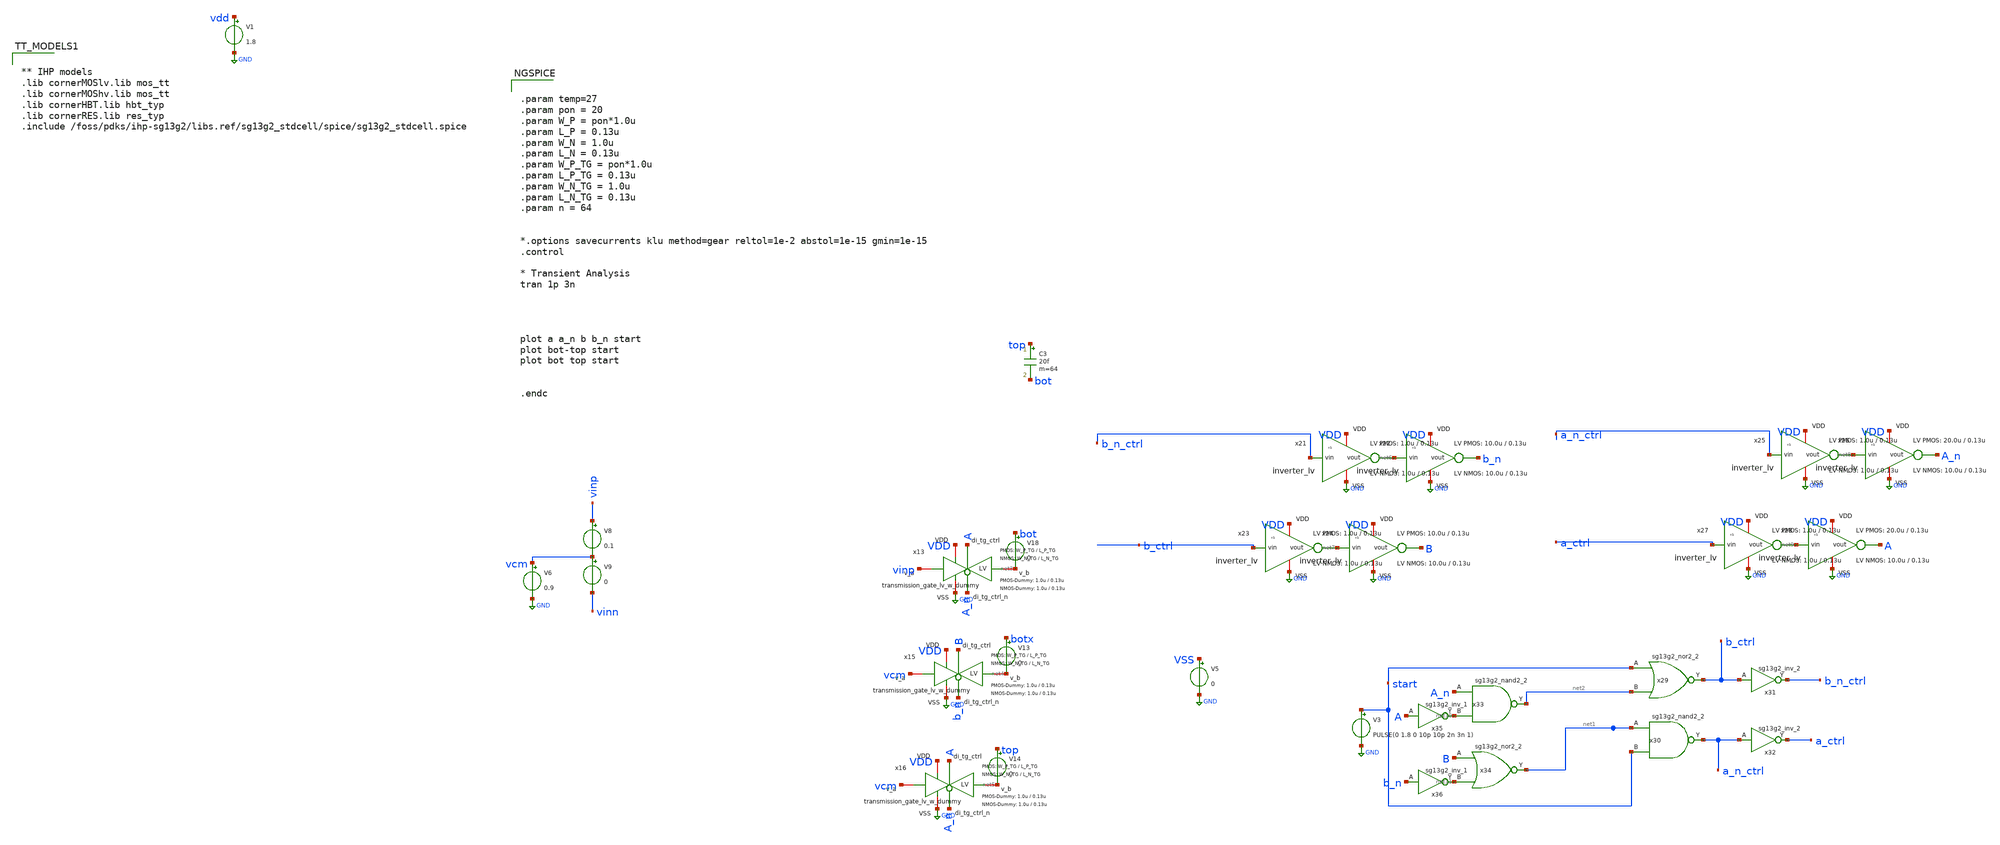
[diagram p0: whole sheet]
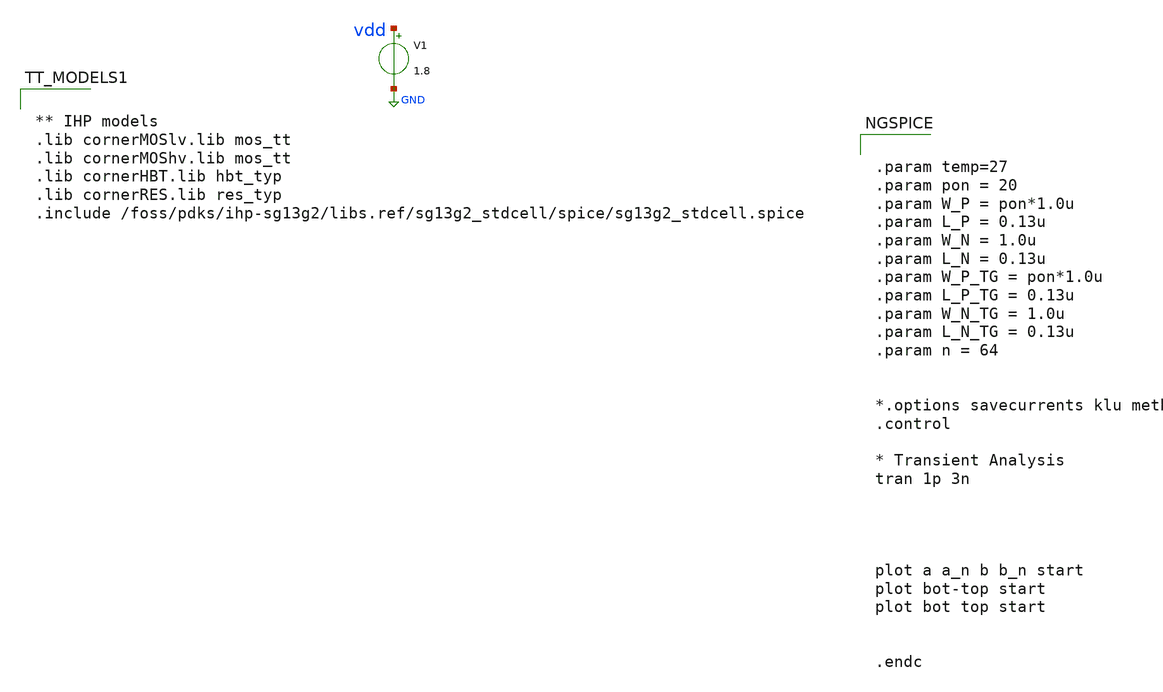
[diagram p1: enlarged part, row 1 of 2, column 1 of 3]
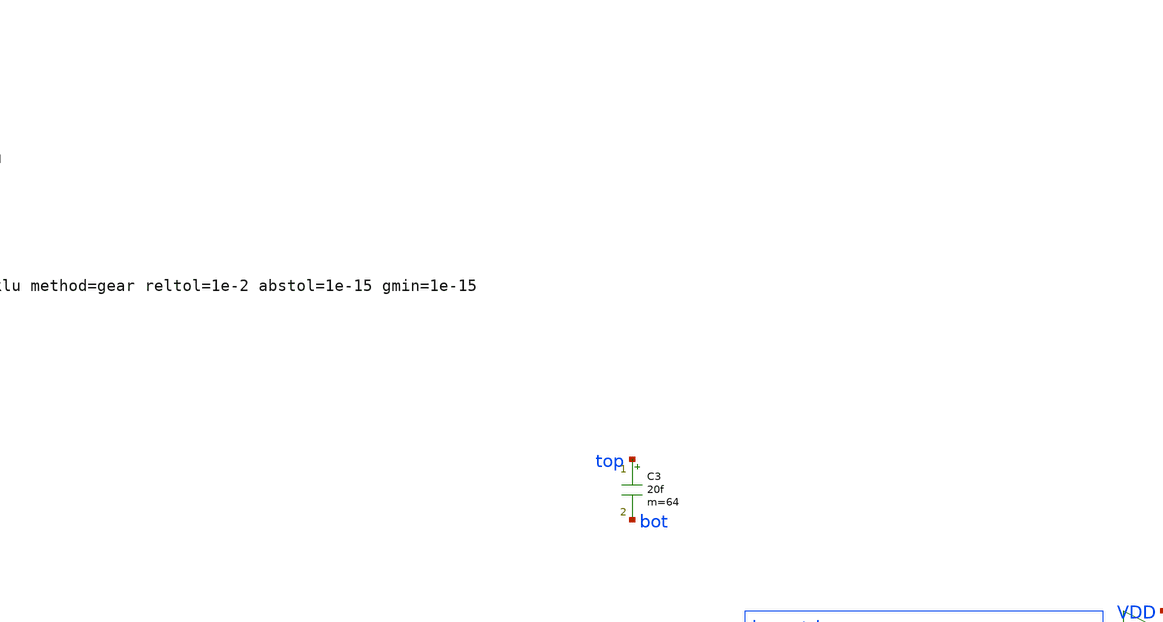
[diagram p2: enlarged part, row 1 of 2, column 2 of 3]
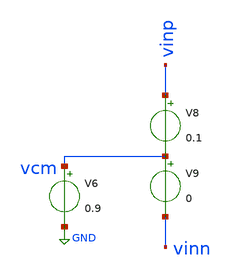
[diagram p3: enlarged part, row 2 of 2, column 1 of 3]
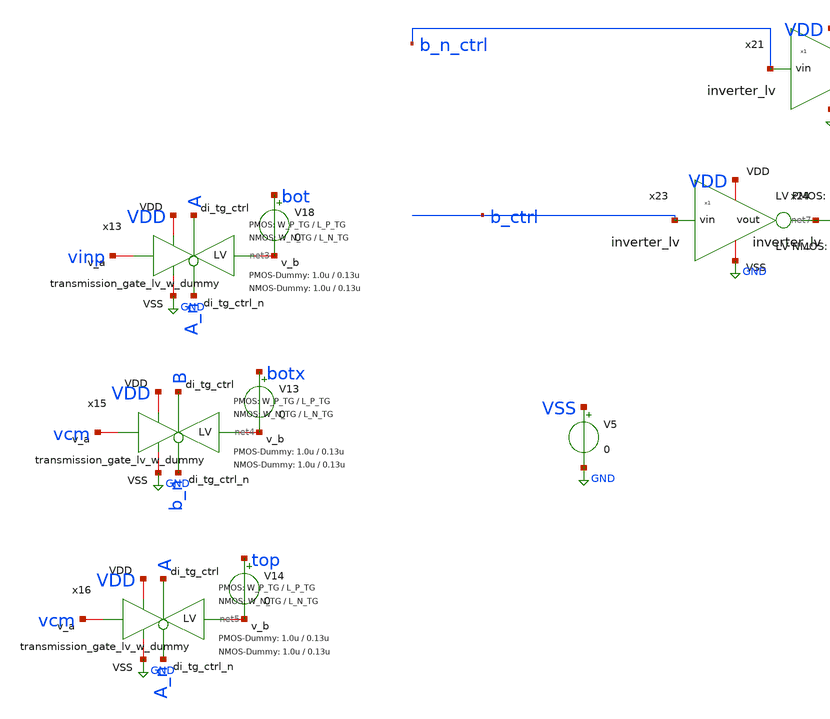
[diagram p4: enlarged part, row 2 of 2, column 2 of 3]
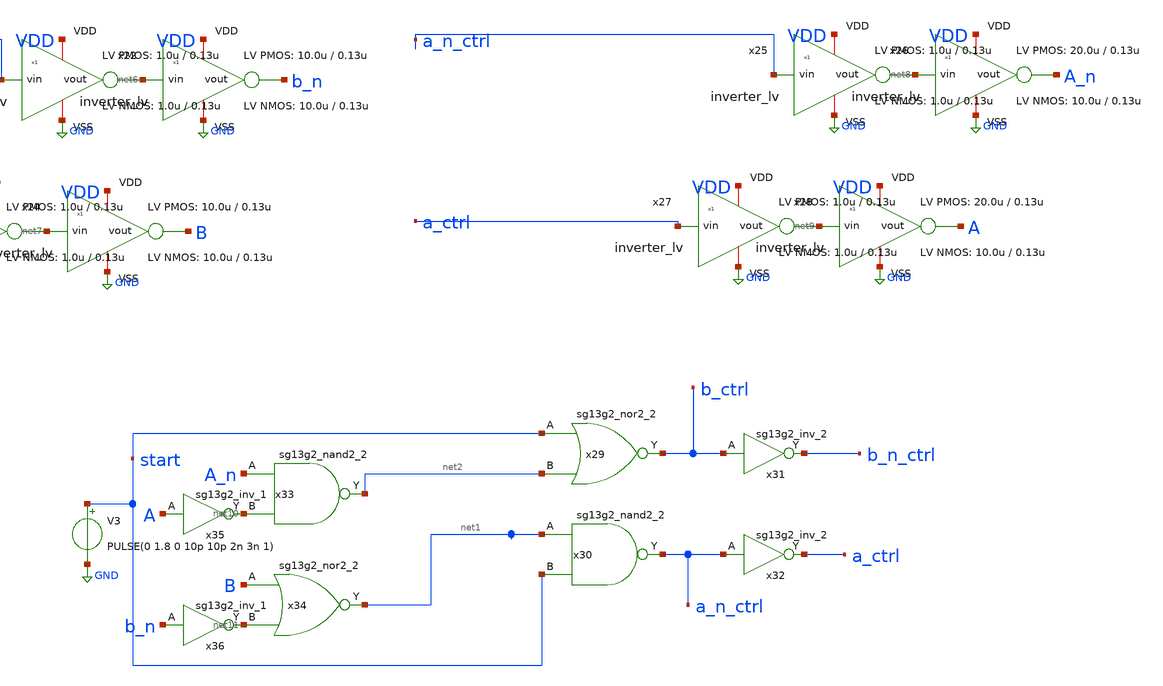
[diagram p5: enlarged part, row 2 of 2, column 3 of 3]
** sch_path: xschem/dac_icms_cell/testbenches/tb_unit_cell_logic_reg_tran_v2 - copia.sch
* IHP-GmbH/IHP-Open-PDK/ihp-sg13g2/libs.tech/xschem/sg13g2_stdcells/sg13g2_inv_2.sch:
* Copyright 2023 IHP PDK Authors
* Licensed under the Apache License, Version 2.0 (the "License");
**.subckt tb_unit_cell_logic_reg_tran_v2 - copia
V1 vdd GND 1.8
V6 vcm GND 0.9
V8 vinp vcm 0.1
x13 VDD A GND net3 vinp A_n transmission_gate_lv_w_dummy W_P=W_P_TG L_P=L_P_TG W_N=W_N_TG L_N=L_N_TG
+ W_P_D=1.0u L_P_D=0.13u W_N_D=1.0u L_N_D=0.13u n=n
V9 vcm vinn 0
x15 VDD B GND net4 vcm b_n transmission_gate_lv_w_dummy W_P=W_P_TG L_P=L_P_TG W_N=W_N_TG L_N=L_N_TG
+ W_P_D=1.0u L_P_D=0.13u W_N_D=1.0u L_N_D=0.13u n=n
x16 VDD A GND net5 vcm A_n transmission_gate_lv_w_dummy W_P=W_P_TG L_P=L_P_TG W_N=W_N_TG L_N=L_N_TG
+ W_P_D=1.0u L_P_D=0.13u W_N_D=1.0u L_N_D=0.13u n=n
V3 start GND PULSE(0 1.8 0 10p 10p 2n 3n 1)
x21 VDD b_n_ctrl net6 GND inverter_lv W_P=1.0u L_P=0.13u W_N=1.0u L_N=0.13u N_C=1
x22 VDD net6 b_n GND inverter_lv W_P=10.0u L_P=0.13u W_N=10.0u L_N=0.13u N_C=1
x23 VDD b_ctrl net7 GND inverter_lv W_P=1.0u L_P=0.13u W_N=1.0u L_N=0.13u N_C=1
x24 VDD net7 B GND inverter_lv W_P=10.0u L_P=0.13u W_N=10.0u L_N=0.13u N_C=1
x25 VDD a_n_ctrl net8 GND inverter_lv W_P=1.0u L_P=0.13u W_N=1.0u L_N=0.13u N_C=1
x26 VDD net8 A_n GND inverter_lv W_P=20.0u L_P=0.13u W_N=10.0u L_N=0.13u N_C=1
x27 VDD a_ctrl net9 GND inverter_lv W_P=1.0u L_P=0.13u W_N=1.0u L_N=0.13u N_C=1
x28 VDD net9 A GND inverter_lv W_P=20.0u L_P=0.13u W_N=10.0u L_N=0.13u N_C=1
x29 b_ctrl start net2 VDD GND sg13g2_nor2_2
x30 a_n_ctrl net1 start VDD GND sg13g2_nand2_2
x31 b_n_ctrl b_ctrl VDD GND sg13g2_inv_2
x32 a_ctrl a_n_ctrl VDD GND sg13g2_inv_2
V5 VSS GND 0
x33 net2 A_n net10 VDD GND sg13g2_nand2_2
x34 net1 B net11 VDD GND sg13g2_nor2_2
x35 net10 A VDD VSS sg13g2_inv_1
x36 net11 b_n VDD VSS sg13g2_inv_1
V13 botx net4 0
V14 top net5 0
V18 bot net3 0
C3 top bot 20f m=64
**** begin user architecture code


.param temp=27
.param pon = 20
.param W_P = pon*1.0u
.param L_P = 0.13u
.param W_N = 1.0u
.param L_N = 0.13u
.param W_P_TG = pon*1.0u
.param L_P_TG = 0.13u
.param W_N_TG = 1.0u
.param L_N_TG = 0.13u
.param n = 64


*.options savecurrents klu method=gear reltol=1e-2 abstol=1e-15 gmin=1e-15
.control

* Transient Analysis
tran 1p 3n




plot a a_n b b_n start
plot bot-top start
plot bot top start


.endc




** IHP models
.lib cornerMOSlv.lib mos_tt
.lib cornerMOShv.lib mos_tt
.lib cornerHBT.lib hbt_typ
.lib cornerRES.lib res_typ
.include /foss/pdks/ihp-sg13g2/libs.ref/sg13g2_stdcell/spice/sg13g2_stdcell.spice


**** end user architecture code
**.ends

* expanding   symbol:  transmission_gate/transmission_gate_lv_w_dummy.sym # of pins=6
** sym_path: xschem/transmission_gate/transmission_gate_lv_w_dummy.sym
** sch_path: xschem/transmission_gate/transmission_gate_lv_w_dummy.sch
.subckt transmission_gate_lv_w_dummy VDD di_tg_ctrl VSS v_b v_a di_tg_ctrl_n  W_P=2.0u L_P=0.13u
+ W_N=2.0u L_N=0.13u W_P_D=1.0u L_P_D=0.13u W_N_D=1.0u L_N_D=0.13u n=1
*.iopin v_a
*.iopin v_b
*.iopin VDD
*.iopin VSS
*.ipin di_tg_ctrl
*.ipin di_tg_ctrl_n
XM1 net3 net5 net4 VSS sg13_lv_nmos w=W_N l=L_N ng=1 m=n mm_ok=1
XM2 net2 net6 net1 VDD sg13_lv_pmos w=W_P l=L_P ng=1 m=n mm_ok=1
XMdummy2 net1 net7 net1 VDD sg13_lv_pmos w=W_P l=L_P ng=1 m={n/2} mm_ok=1
XMdummy1 net4 net8 net4 VSS sg13_lv_nmos w=W_N l=L_N ng=1 m={n/2} mm_ok=1
Vig1 di_tg_ctrl net5 0
Vig2 di_tg_ctrl_n net6 0
Vig1d di_tg_ctrl_n net8 0
Vig2d di_tg_ctrl net7 0
Vid2 v_a net2 0
Vid1 v_a net3 0
Vis2 v_b net1 0
Vis1 v_b net4 0
.ends


* expanding   symbol:  inverter/inverter_lv.sym # of pins=4
** sym_path: xschem/inverter/inverter_lv.sym
** sch_path: xschem/inverter/inverter_lv.sch
.subckt inverter_lv VDD vin vout VSS  W_P=3.0u L_P=0.13u W_N=1.0u L_N=0.13u N_C=1
*.ipin vin
*.iopin VDD
*.iopin VSS
*.opin vout
XM1 vout vin VDD VDD sg13_lv_pmos w=W_P l=L_P ng=1 m={N_C} mm_ok=1
XM2 vout vin VSS VSS sg13_lv_nmos w=W_N l=L_N ng=1 m={N_C} mm_ok=1
.ends


* expanding   symbol:  sg13g2_stdcells/sg13g2_nor2_2.sym # of pins=3
** sym_path: sg13g2_stdcells/sg13g2_nor2_2.sym
** sch_path: sg13g2_stdcells/sg13g2_nor2_2.sch
.subckt sg13g2_nor2_2 Y A B VDD VSS
*.opin Y
*.ipin B
*.ipin A
*.iopin VDD
*.iopin VSS
XM1 Y A VSS VSS sg13_lv_nmos w=1.48u l=130.00n ng=2 m=1 mm_ok=1
XM2 Y B VSS VSS sg13_lv_nmos w=1.48u l=130.00n ng=2 m=1 mm_ok=1
XM3 net1 A VDD VDD sg13_lv_pmos w=2.24u l=130.00n ng=2 m=1 mm_ok=1
XM4 Y B net1 VDD sg13_lv_pmos w=2.24u l=130.00n ng=2 m=1 mm_ok=1
.ends


* expanding   symbol:  sg13g2_stdcells/sg13g2_nand2_2.sym # of pins=3
** sym_path: sg13g2_stdcells/sg13g2_nand2_2.sym
** sch_path: sg13g2_stdcells/sg13g2_nand2_2.sch
.subckt sg13g2_nand2_2 Y A B VDD VSS
*.iopin VDD
*.iopin VSS
*.opin Y
*.ipin B
*.ipin A
XM1 Y A net1 VSS sg13_lv_nmos w=1.44u l=130.00n ng=2 m=1 mm_ok=1
XM2 net1 B VSS VSS sg13_lv_nmos w=1.44u l=130.00n ng=2 m=1 mm_ok=1
XM3 Y A VDD VDD sg13_lv_pmos w=2.24u l=130.00n ng=2 m=1 mm_ok=1
XM4 Y B VDD VDD sg13_lv_pmos w=2.24u l=130.00n ng=2 m=1 mm_ok=1
.ends


* expanding   symbol:  sg13g2_stdcells/sg13g2_inv_2.sym # of pins=2
** sym_path: sg13g2_stdcells/sg13g2_inv_2.sym
** sch_path: sg13g2_stdcells/sg13g2_inv_2.sch
.subckt sg13g2_inv_2 Y A VDD VSS
*.opin Y
*.ipin A
*.iopin VDD
*.iopin VSS
XM1 Y A VSS VSS sg13_lv_nmos w=1.48u l=130.00n ng=2 m=1 mm_ok=1
XM2 Y A VDD VDD sg13_lv_pmos w=2.24u l=130.00n ng=2 m=1 mm_ok=1
.ends


* expanding   symbol:  sg13g2_stdcells/sg13g2_inv_1.sym # of pins=2
** sym_path: sg13g2_stdcells/sg13g2_inv_1.sym
** sch_path: sg13g2_stdcells/sg13g2_inv_1.sch
.subckt sg13g2_inv_1 Y A VDD VSS
*.opin Y
*.ipin A
*.iopin VDD
*.iopin VSS
XM1 Y A VSS VSS sg13_lv_nmos w=740.00n l=130.00n ng=1 m=1 mm_ok=1
XM2 Y A VDD VDD sg13_lv_pmos w=1.12u l=130.00n ng=1 m=1 mm_ok=1
.ends

.GLOBAL GND
.end
